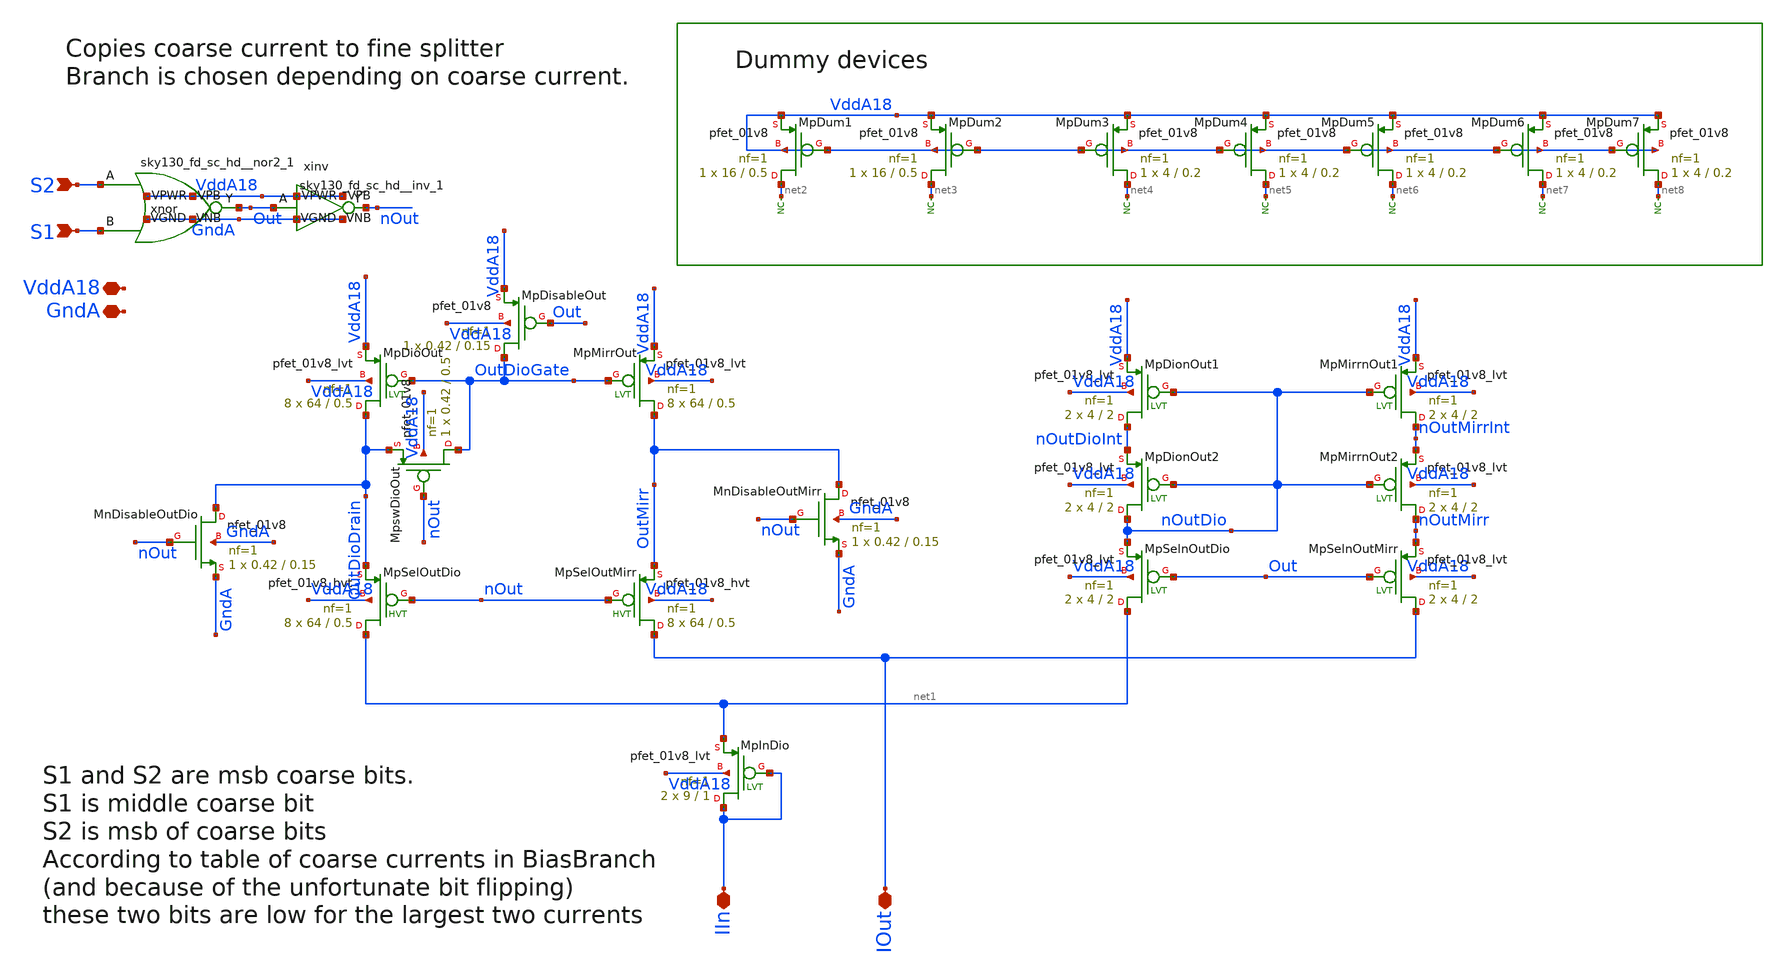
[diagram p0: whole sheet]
** sch_path: analog/xschem/BiasCoarseFineInterface_omowuyi.sch
**.subckt BiasCoarseFineInterface_omowuyi GndA VddA18 IIn IOut S2 S1
*.iopin GndA
*.iopin VddA18
*.iopin IIn
*.iopin IOut
*.ipin S2
*.ipin S1
XMpDisableOut OutDioGate Out VddA18 VddA18 sky130_fd_pr__pfet_01v8 L=0.15 W=0.42 nf=1 ad='int((1 + 1)/2) * 0.42 / 1 * 0.29'
+ as='int((1 + 2)/2) * 0.42 / 1 * 0.29' pd='2*int((1 + 1)/2) * (0.42 / 1 + 0.29)' ps='2*int((1 + 2)/2) * (0.42 / 1 + 0.29)'
+ nrd='0.29 / 0.42 ' nrs='0.29 / 0.42 ' sa=0 sb=0 sd=0 mult=1 m=1
XMpDioOut OutDioDrain OutDioGate VddA18 VddA18 sky130_fd_pr__pfet_01v8_lvt L=0.5 W=64 nf=1 ad='int((1 + 1)/2) * 64 / 1 * 0.29'
+ as='int((1 + 2)/2) * 64 / 1 * 0.29' pd='2*int((1 + 1)/2) * (64 / 1 + 0.29)' ps='2*int((1 + 2)/2) * (64 / 1 + 0.29)'
+ nrd='0.29 / 64 ' nrs='0.29 / 64 ' sa=0 sb=0 sd=0 mult=8 m=8
XMpMirrOut OutMirr OutDioGate VddA18 VddA18 sky130_fd_pr__pfet_01v8_lvt L=0.5 W=64 nf=1 ad='int((1 + 1)/2) * 64 / 1 * 0.29'
+ as='int((1 + 2)/2) * 64 / 1 * 0.29' pd='2*int((1 + 1)/2) * (64 / 1 + 0.29)' ps='2*int((1 + 2)/2) * (64 / 1 + 0.29)'
+ nrd='0.29 / 64 ' nrs='0.29 / 64 ' sa=0 sb=0 sd=0 mult=8 m=8
XMpswDioOut OutDioGate nOut OutDioDrain VddA18 sky130_fd_pr__pfet_01v8 L=0.5 W=0.42 nf=1 ad='int((1 + 1)/2) * 0.42 / 1 * 0.29'
+ as='int((1 + 2)/2) * 0.42 / 1 * 0.29' pd='2*int((1 + 1)/2) * (0.42 / 1 + 0.29)' ps='2*int((1 + 2)/2) * (0.42 / 1 + 0.29)'
+ nrd='0.29 / 0.42 ' nrs='0.29 / 0.42 ' sa=0 sb=0 sd=0 mult=1 m=1
XMnDisableOutDio OutDioDrain nOut GndA GndA sky130_fd_pr__nfet_01v8 L=0.15 W=0.42 nf=1 ad='int((1 + 1)/2) * 0.42 / 1 * 0.29'
+ as='int((1 + 2)/2) * 0.42 / 1 * 0.29' pd='2*int((1 + 1)/2) * (0.42 / 1 + 0.29)' ps='2*int((1 + 2)/2) * (0.42 / 1 + 0.29)'
+ nrd='0.29 / 0.42 ' nrs='0.29 / 0.42 ' sa=0 sb=0 sd=0 mult=1 m=1
XMpSelOutDio net1 nOut OutDioDrain VddA18 sky130_fd_pr__pfet_01v8_hvt L=0.5 W=64 nf=1 ad='int((1 + 1)/2) * 64 / 1 * 0.29'
+ as='int((1 + 2)/2) * 64 / 1 * 0.29' pd='2*int((1 + 1)/2) * (64 / 1 + 0.29)' ps='2*int((1 + 2)/2) * (64 / 1 + 0.29)'
+ nrd='0.29 / 64 ' nrs='0.29 / 64 ' sa=0 sb=0 sd=0 mult=8 m=8
XMpSelOutMirr IOut nOut OutMirr VddA18 sky130_fd_pr__pfet_01v8_hvt L=0.5 W=64 nf=1 ad='int((1 + 1)/2) * 64 / 1 * 0.29'
+ as='int((1 + 2)/2) * 64 / 1 * 0.29' pd='2*int((1 + 1)/2) * (64 / 1 + 0.29)' ps='2*int((1 + 2)/2) * (64 / 1 + 0.29)'
+ nrd='0.29 / 64 ' nrs='0.29 / 64 ' sa=0 sb=0 sd=0 mult=8 m=8
XMnDisableOutMirr OutMirr nOut GndA GndA sky130_fd_pr__nfet_01v8 L=0.15 W=0.42 nf=1 ad='int((1 + 1)/2) * 0.42 / 1 * 0.29'
+ as='int((1 + 2)/2) * 0.42 / 1 * 0.29' pd='2*int((1 + 1)/2) * (0.42 / 1 + 0.29)' ps='2*int((1 + 2)/2) * (0.42 / 1 + 0.29)'
+ nrd='0.29 / 0.42 ' nrs='0.29 / 0.42 ' sa=0 sb=0 sd=0 mult=1 m=1
XMpInDio IIn IIn net1 VddA18 sky130_fd_pr__pfet_01v8_lvt L=1 W=9 nf=1 ad='int((1 + 1)/2) * 9 / 1 * 0.29'
+ as='int((1 + 2)/2) * 9 / 1 * 0.29' pd='2*int((1 + 1)/2) * (9 / 1 + 0.29)' ps='2*int((1 + 2)/2) * (9 / 1 + 0.29)'
+ nrd='0.29 / 9 ' nrs='0.29 / 9 ' sa=0 sb=0 sd=0 mult=2 m=2
XMpDionOut1 nOutDioInt nOutDio VddA18 VddA18 sky130_fd_pr__pfet_01v8_lvt L=2 W=4 nf=1 ad='int((1 + 1)/2) * 4 / 1 * 0.29'
+ as='int((1 + 2)/2) * 4 / 1 * 0.29' pd='2*int((1 + 1)/2) * (4 / 1 + 0.29)' ps='2*int((1 + 2)/2) * (4 / 1 + 0.29)'
+ nrd='0.29 / 4 ' nrs='0.29 / 4 ' sa=0 sb=0 sd=0 mult=2 m=2
XMpMirrnOut1 nOutMirrInt nOutDio VddA18 VddA18 sky130_fd_pr__pfet_01v8_lvt L=2 W=4 nf=1 ad='int((1 + 1)/2) * 4 / 1 * 0.29'
+ as='int((1 + 2)/2) * 4 / 1 * 0.29' pd='2*int((1 + 1)/2) * (4 / 1 + 0.29)' ps='2*int((1 + 2)/2) * (4 / 1 + 0.29)'
+ nrd='0.29 / 4 ' nrs='0.29 / 4 ' sa=0 sb=0 sd=0 mult=2 m=2
XMpDionOut2 nOutDio nOutDio nOutDioInt VddA18 sky130_fd_pr__pfet_01v8_lvt L=2 W=4 nf=1 ad='int((1 + 1)/2) * 4 / 1 * 0.29'
+ as='int((1 + 2)/2) * 4 / 1 * 0.29' pd='2*int((1 + 1)/2) * (4 / 1 + 0.29)' ps='2*int((1 + 2)/2) * (4 / 1 + 0.29)'
+ nrd='0.29 / 4 ' nrs='0.29 / 4 ' sa=0 sb=0 sd=0 mult=2 m=2
XMpMirrnOut2 nOutMirr nOutDio nOutMirrInt VddA18 sky130_fd_pr__pfet_01v8_lvt L=2 W=4 nf=1 ad='int((1 + 1)/2) * 4 / 1 * 0.29'
+ as='int((1 + 2)/2) * 4 / 1 * 0.29' pd='2*int((1 + 1)/2) * (4 / 1 + 0.29)' ps='2*int((1 + 2)/2) * (4 / 1 + 0.29)'
+ nrd='0.29 / 4 ' nrs='0.29 / 4 ' sa=0 sb=0 sd=0 mult=2 m=2
XMpDum1 net2 VddA18 VddA18 VddA18 sky130_fd_pr__pfet_01v8 L=0.5 W=16 nf=1 ad='int((1 + 1)/2) * 16 / 1 * 0.29'
+ as='int((1 + 2)/2) * 16 / 1 * 0.29' pd='2*int((1 + 1)/2) * (16 / 1 + 0.29)' ps='2*int((1 + 2)/2) * (16 / 1 + 0.29)'
+ nrd='0.29 / 16 ' nrs='0.29 / 16 ' sa=0 sb=0 sd=0 mult=1 m=1
XMpDum2 net3 VddA18 VddA18 VddA18 sky130_fd_pr__pfet_01v8 L=0.5 W=16 nf=1 ad='int((1 + 1)/2) * 16 / 1 * 0.29'
+ as='int((1 + 2)/2) * 16 / 1 * 0.29' pd='2*int((1 + 1)/2) * (16 / 1 + 0.29)' ps='2*int((1 + 2)/2) * (16 / 1 + 0.29)'
+ nrd='0.29 / 16 ' nrs='0.29 / 16 ' sa=0 sb=0 sd=0 mult=1 m=1
XMpDum3 net4 VddA18 VddA18 VddA18 sky130_fd_pr__pfet_01v8 L=0.2 W=4 nf=1 ad='int((1 + 1)/2) * 4 / 1 * 0.29'
+ as='int((1 + 2)/2) * 4 / 1 * 0.29' pd='2*int((1 + 1)/2) * (4 / 1 + 0.29)' ps='2*int((1 + 2)/2) * (4 / 1 + 0.29)'
+ nrd='0.29 / 4 ' nrs='0.29 / 4 ' sa=0 sb=0 sd=0 mult=1 m=1
XMpDum4 net5 VddA18 VddA18 VddA18 sky130_fd_pr__pfet_01v8 L=0.2 W=4 nf=1 ad='int((1 + 1)/2) * 4 / 1 * 0.29'
+ as='int((1 + 2)/2) * 4 / 1 * 0.29' pd='2*int((1 + 1)/2) * (4 / 1 + 0.29)' ps='2*int((1 + 2)/2) * (4 / 1 + 0.29)'
+ nrd='0.29 / 4 ' nrs='0.29 / 4 ' sa=0 sb=0 sd=0 mult=1 m=1
XMpDum5 net6 VddA18 VddA18 VddA18 sky130_fd_pr__pfet_01v8 L=0.2 W=4 nf=1 ad='int((1 + 1)/2) * 4 / 1 * 0.29'
+ as='int((1 + 2)/2) * 4 / 1 * 0.29' pd='2*int((1 + 1)/2) * (4 / 1 + 0.29)' ps='2*int((1 + 2)/2) * (4 / 1 + 0.29)'
+ nrd='0.29 / 4 ' nrs='0.29 / 4 ' sa=0 sb=0 sd=0 mult=1 m=1
XMpDum6 net7 VddA18 VddA18 VddA18 sky130_fd_pr__pfet_01v8 L=0.2 W=4 nf=1 ad='int((1 + 1)/2) * 4 / 1 * 0.29'
+ as='int((1 + 2)/2) * 4 / 1 * 0.29' pd='2*int((1 + 1)/2) * (4 / 1 + 0.29)' ps='2*int((1 + 2)/2) * (4 / 1 + 0.29)'
+ nrd='0.29 / 4 ' nrs='0.29 / 4 ' sa=0 sb=0 sd=0 mult=1 m=1
XMpDum7 net8 VddA18 VddA18 VddA18 sky130_fd_pr__pfet_01v8 L=0.2 W=4 nf=1 ad='int((1 + 1)/2) * 4 / 1 * 0.29'
+ as='int((1 + 2)/2) * 4 / 1 * 0.29' pd='2*int((1 + 1)/2) * (4 / 1 + 0.29)' ps='2*int((1 + 2)/2) * (4 / 1 + 0.29)'
+ nrd='0.29 / 4 ' nrs='0.29 / 4 ' sa=0 sb=0 sd=0 mult=1 m=1
* noconn #net2
* noconn #net3
* noconn #net4
* noconn #net5
* noconn #net6
* noconn #net7
* noconn #net8
xnor S2 S1 Out VddA18 VddA18 GndA GndA sky130_fd_sc_hd__nor2_1
xinv Out nOut VddA18 VddA18 GndA GndA sky130_fd_sc_hd__inv_1
XMpSelnOutDio net1 Out nOutDio VddA18 sky130_fd_pr__pfet_01v8_lvt L=2 W=4 nf=1 ad='int((1 + 1)/2) * 4 / 1 * 0.29'
+ as='int((1 + 2)/2) * 4 / 1 * 0.29' pd='2*int((1 + 1)/2) * (4 / 1 + 0.29)' ps='2*int((1 + 2)/2) * (4 / 1 + 0.29)'
+ nrd='0.29 / 4 ' nrs='0.29 / 4 ' sa=0 sb=0 sd=0 mult=2 m=2
XMpSelnOutMirr IOut Out nOutMirr VddA18 sky130_fd_pr__pfet_01v8_lvt L=2 W=4 nf=1 ad='int((1 + 1)/2) * 4 / 1 * 0.29'
+ as='int((1 + 2)/2) * 4 / 1 * 0.29' pd='2*int((1 + 1)/2) * (4 / 1 + 0.29)' ps='2*int((1 + 2)/2) * (4 / 1 + 0.29)'
+ nrd='0.29 / 4 ' nrs='0.29 / 4 ' sa=0 sb=0 sd=0 mult=2 m=2
**.ends
.end
